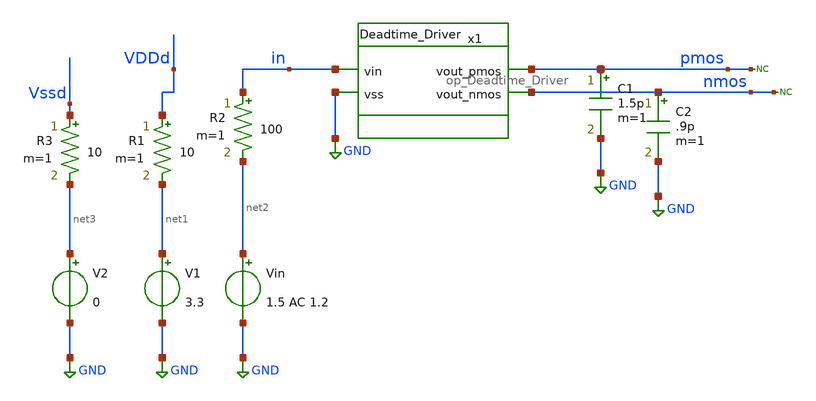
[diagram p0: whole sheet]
** sch_path: designs/libs/tb_analog/tb_op_Deadtime_Driver/tb_op_deadtime_driver.sch
**.subckt tb_op_deadtime_driver
V1 net1 GND 3.3
Vin net2 GND 1.5 AC 1.2
R1 VDDd net1 10 m=1
R2 in net2 100 m=1
V2 net3 GND 0
* noconn pmos
* noconn nmos
x1 pmos in nmos GND op_Deadtime_Driver
R3 Vssd net3 10 m=1
C1 pmos GND 1.5p m=1
C2 nmos GND .9p m=1
**** begin user architecture code

.include $::180MCU_MODELS/design.ngspice
.include /foss/pdks/gf180mcuD/libs.ref/gf180mcu_fd_sc_mcu9t5v0/spice/gf180mcu_fd_sc_mcu9t5v0.spice
.lib $::180MCU_MODELS/sm141064.ngspice typical
.lib $::180MCU_MODELS/sm141064.ngspice cap_mim
.lib $::180MCU_MODELS/sm141064.ngspice mimcap_typical




.global VDDd VSSd
.control
save all
**Frequency & time settings
let fsig = 200k
let tper=1/fsig
let tfr = 0.01*tper
let ton = 0.5*tper-2*tfr

let tstop = 4 * tper
let tstep = 0.001*tper


**voltages
alter @Vin[PULSE] = [ 0 2.3 0 $&tfr $&tfr $&ton $&tper 3 ]
alter @Vin[DC] = 0
*alter @Vin[SIN] = [ 1.7 1.5 $&fsig 0 0 ]

**simulation
OP
*show all > op.log
show all

**Basic performance analysis
tran $&tstep $&tstop

**Rise and Fall time for delay checking
meas tran trise_p TRIG v(pmos) VAL=0.66 RISE=3 TARG v(pmos) VAL=3.0 RISE=3
meas tran trise_n TRIG v(nmos) VAL=0.66 RISE=3 TARG v(nmos) VAL=3.0 RISE=3

meas tran tfall_p TRIG v(pmos) VAL=3.0 FALL=3 TARG v(pmos) VAL=0.66 FALL=3
meas tran tfall_n TRIG v(nmos) VAL=3.0 FALL=3 TARG v(nmos) VAL=0.66 FALL=3

plot nmos pmos

**Buffer overshoot checker

meas tran nmos_min MIN v(nmos)
meas tran nmos_max MAX v(nmos)

**AC simulation
*AC dec 100 1 10e6
*plot db(v(nmos)) db(v(pmos))
*plot 180*cph(v(nmos))/pi 180*cph(v(pmos))/pi



write Deadtime_Driver_tb.raw
.endc


**** end user architecture code
**.ends
.GLOBAL GND
.end
